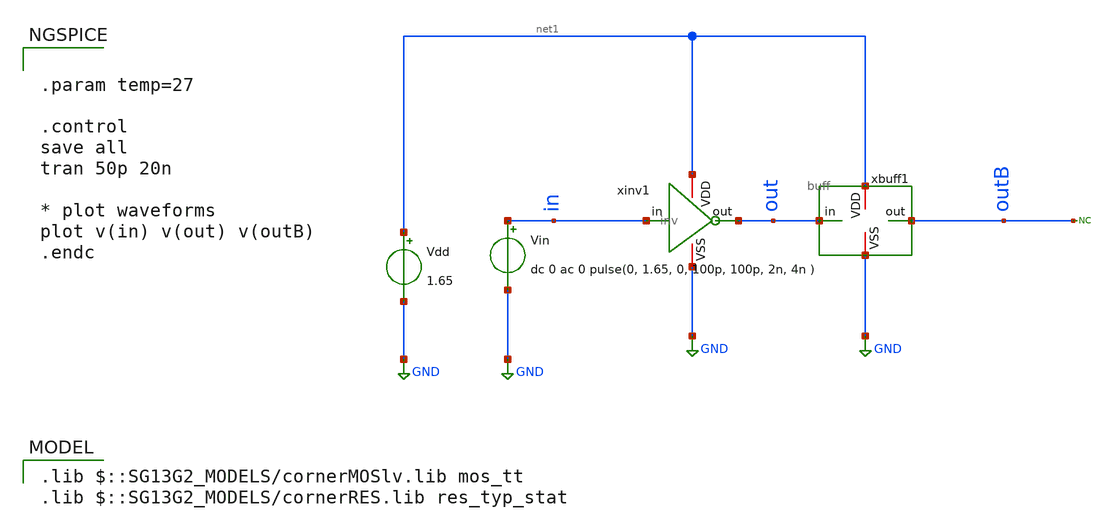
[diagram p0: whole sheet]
** sch_path: blocks/composite/dpi_adexp_neuron/design_data/xschem/buffer_tb.sch
**.subckt buffer_tb
Vdd net1 GND 1.65
Vin in GND dc 0 ac 0 pulse(0, 1.65, 0, 100p, 100p, 2n, 4n )
xinv1 net1 in out GND inv
xbuff1 net1 out outB GND buff
* noconn outB
**** begin user architecture code


.param temp=27

.control
save all
tran 50p 20n

* plot waveforms
plot v(in) v(out) v(outB)
.endc



 .lib $::SG13G2_MODELS/cornerMOSlv.lib mos_tt
.lib $::SG13G2_MODELS/cornerRES.lib res_typ_stat

**** end user architecture code
**.ends
.GLOBAL GND
.end
